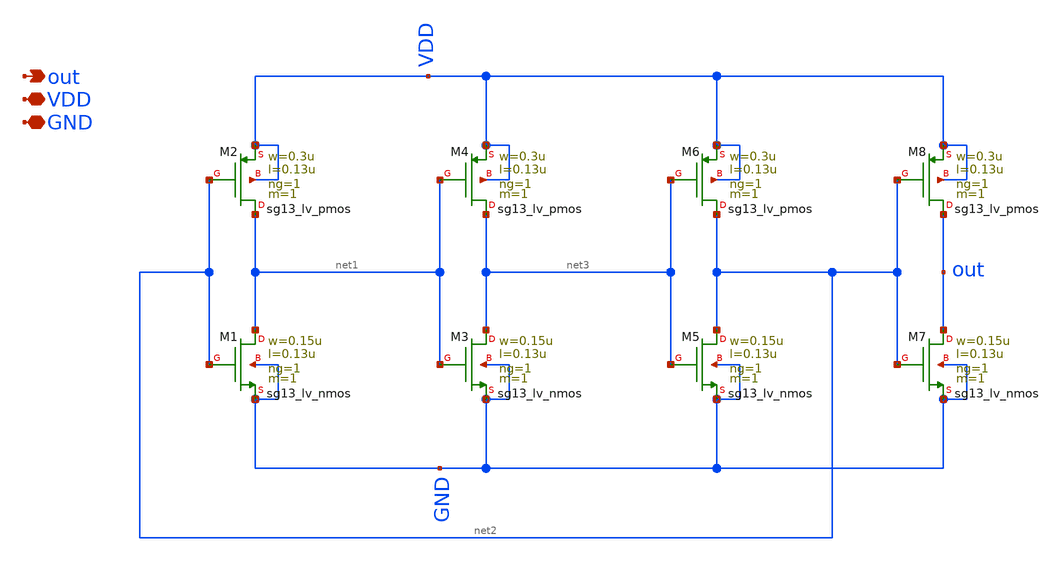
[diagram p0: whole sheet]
** sch_path: 20260719_tunnable_ring_oscillator/ro3.sch
**.subckt ro3 out VDD GND
*.opin out
*.iopin VDD
*.iopin GND
XM1 net1 net2 GND GND sg13_lv_nmos w=0.15u l=0.13u ng=1 m=1 mm_ok=1
XM2 net1 net2 VDD VDD sg13_lv_pmos w=0.3u l=0.13u ng=1 m=1 mm_ok=1
XM3 net3 net1 GND GND sg13_lv_nmos w=0.15u l=0.13u ng=1 m=1 mm_ok=1
XM4 net3 net1 VDD VDD sg13_lv_pmos w=0.3u l=0.13u ng=1 m=1 mm_ok=1
XM5 net2 net3 GND GND sg13_lv_nmos w=0.15u l=0.13u ng=1 m=1 mm_ok=1
XM6 net2 net3 VDD VDD sg13_lv_pmos w=0.3u l=0.13u ng=1 m=1 mm_ok=1
XM7 out net2 GND GND sg13_lv_nmos w=0.15u l=0.13u ng=1 m=1 mm_ok=1
XM8 out net2 VDD VDD sg13_lv_pmos w=0.3u l=0.13u ng=1 m=1 mm_ok=1
**.ends
.end
